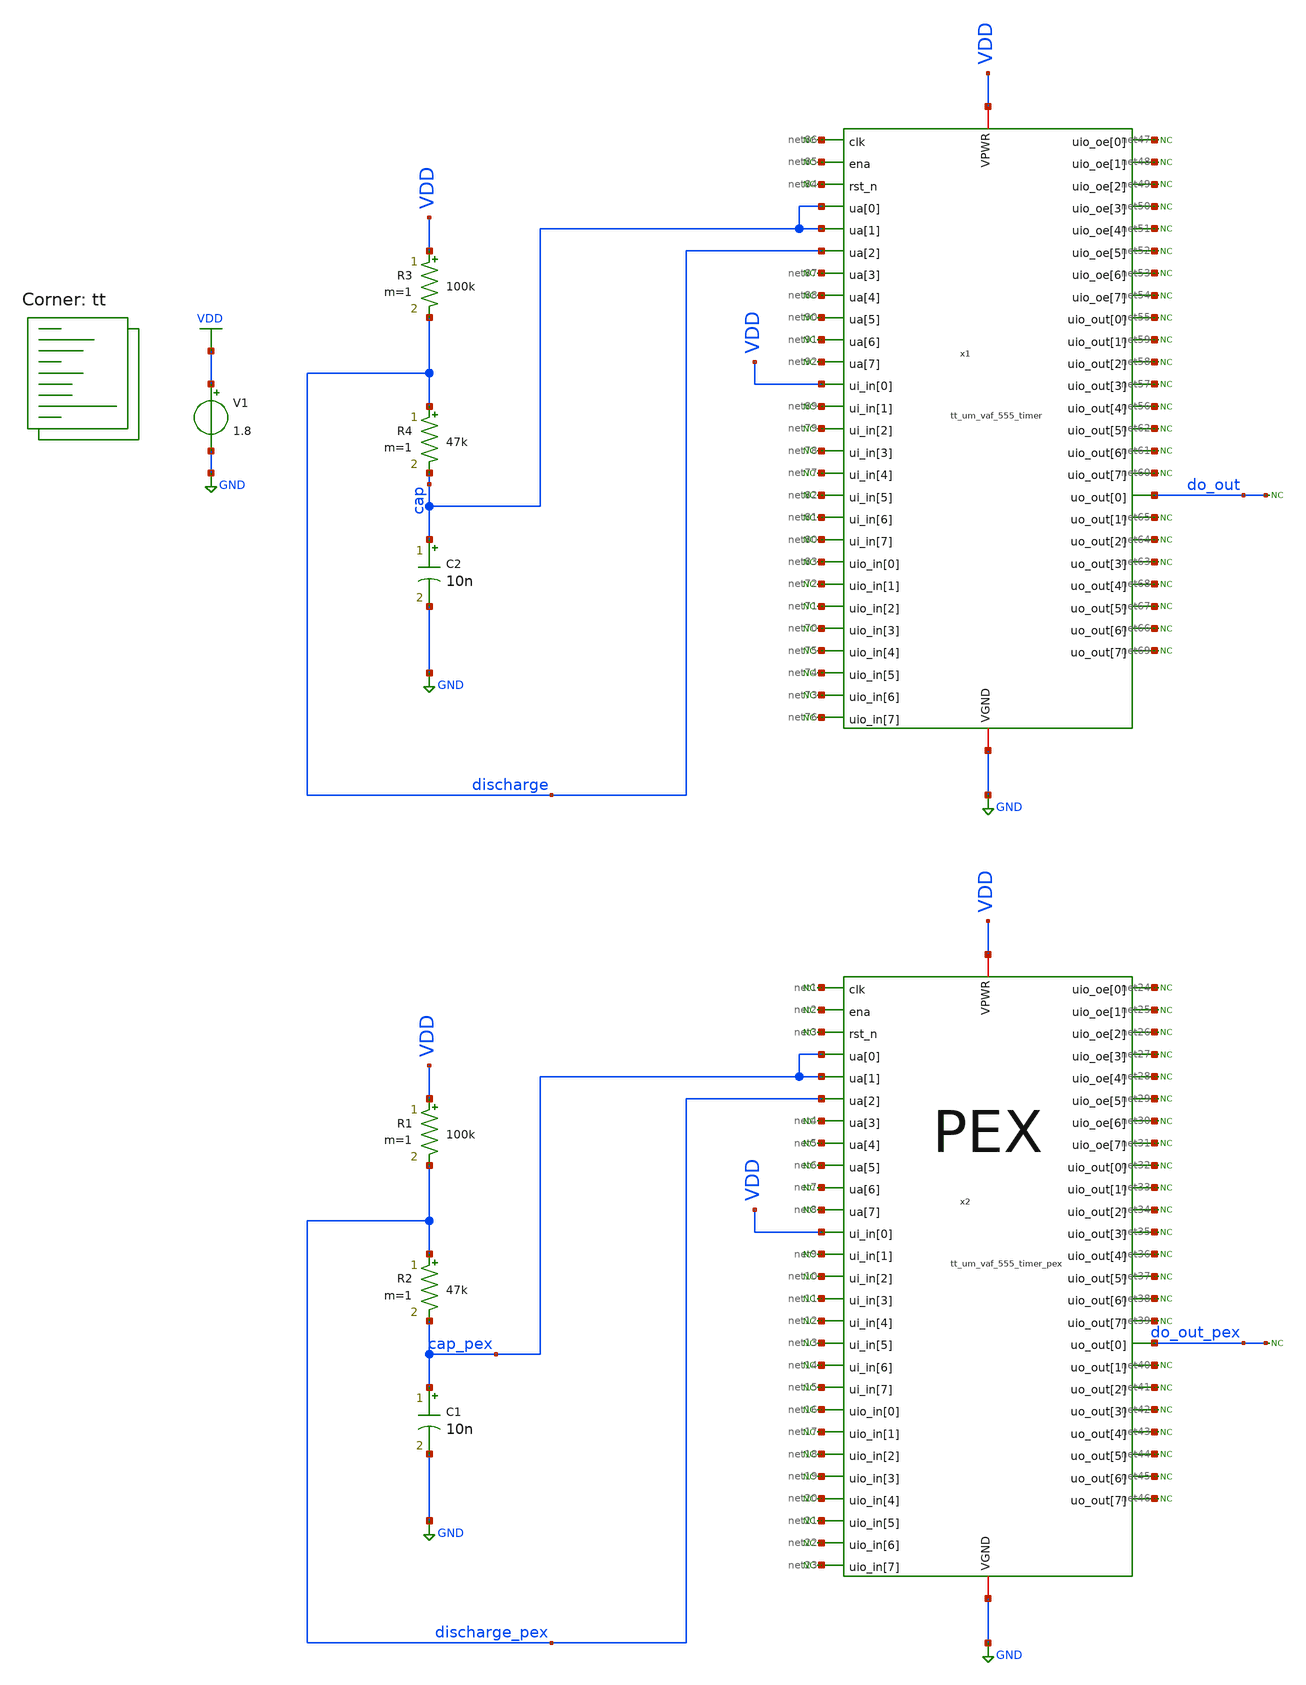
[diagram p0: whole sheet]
** sch_path: xsch/tb/tt_um_vaf_555_timer/tb_tt_um_vaf_555_timer_astable.sch
**.subckt tb_tt_um_vaf_555_timer_astable
V1 VDD GND 1.8
.save i(v1)
x2 net1 net2 net3 cap_pex cap_pex discharge_pex net4 net5 net6 net7 net8 VDD net9 net10 net11 net12
+ net13 net14 net15 net16 net17 net18 net19 net20 net21 net22 net23 net24 net25 net26 net27 net28 net29
+ net30 net31 net32 net33 net34 net35 net36 net37 net38 net39 do_out_pex net40 net41 net42 net43 net44
+ net45 net46 VDD GND tt_um_vaf_555_timer_pex
R3 VDD discharge 100k m=1
R4 discharge cap 47k m=1
C2 cap GND 10n m=1
* noconn do_out
* noconn #net47
* noconn #net48
* noconn #net49
* noconn #net50
* noconn #net51
* noconn #net52
* noconn #net53
* noconn #net54
* noconn #net55
* noconn #net56
* noconn #net57
* noconn #net58
* noconn #net59
* noconn #net60
* noconn #net61
* noconn #net62
* noconn #net63
* noconn #net64
* noconn #net65
* noconn #net66
* noconn #net67
* noconn #net68
* noconn #net69
* noconn #net70
* noconn #net71
* noconn #net72
* noconn #net73
* noconn #net74
* noconn #net75
* noconn #net76
* noconn #net77
* noconn #net78
* noconn #net79
* noconn #net80
* noconn #net81
* noconn #net82
* noconn #net83
* noconn #net84
* noconn #net85
* noconn #net86
* noconn #net87
* noconn #net88
* noconn #net89
x1 net86 net85 net84 cap cap discharge net87 net88 net90 net91 net92 VDD net89 net79 net78 net77
+ net82 net81 net80 net83 net72 net71 net70 net75 net74 net73 net76 net47 net48 net49 net50 net51 net52
+ net53 net54 net55 net59 net58 net57 net56 net62 net61 net60 do_out net65 net64 net63 net68 net67 net66
+ net69 VDD GND tt_um_vaf_555_timer
* noconn #net90
* noconn #net91
* noconn #net92
R1 VDD discharge_pex 100k m=1
R2 discharge_pex cap_pex 47k m=1
C1 cap_pex GND 10n m=1
* noconn do_out_pex
* noconn #net24
* noconn #net25
* noconn #net26
* noconn #net27
* noconn #net28
* noconn #net29
* noconn #net30
* noconn #net31
* noconn #net32
* noconn #net36
* noconn #net35
* noconn #net34
* noconn #net33
* noconn #net39
* noconn #net38
* noconn #net37
* noconn #net42
* noconn #net41
* noconn #net40
* noconn #net45
* noconn #net44
* noconn #net43
* noconn #net46
* noconn #net19
* noconn #net18
* noconn #net17
* noconn #net22
* noconn #net21
* noconn #net20
* noconn #net23
* noconn #net12
* noconn #net11
* noconn #net10
* noconn #net15
* noconn #net14
* noconn #net13
* noconn #net16
* noconn #net3
* noconn #net2
* noconn #net1
* noconn #net4
* noconn #net5
* noconn #net9
* noconn #net6
* noconn #net7
* noconn #net8
**** begin user architecture code



.ic v(cap) = 0
.ic v(cap_pex) = 0

.control
	tran 1u 10m

	plot v(cap) v(cap_pex)

.endc
.end


.lib $::SKYWATER_MODELS/sky130.lib.spice tt


.save v(do_out) v(discharge) v(cap) v(cap_pex)
=

.savecurrents




.include ~/projects/tt06_555/xsch/ip/top/tt_um_vaf_555_timer/tt_um_vaf_555_timer_pex.spice


**** end user architecture code
**.ends
.GLOBAL VDD
.GLOBAL GND
.end
